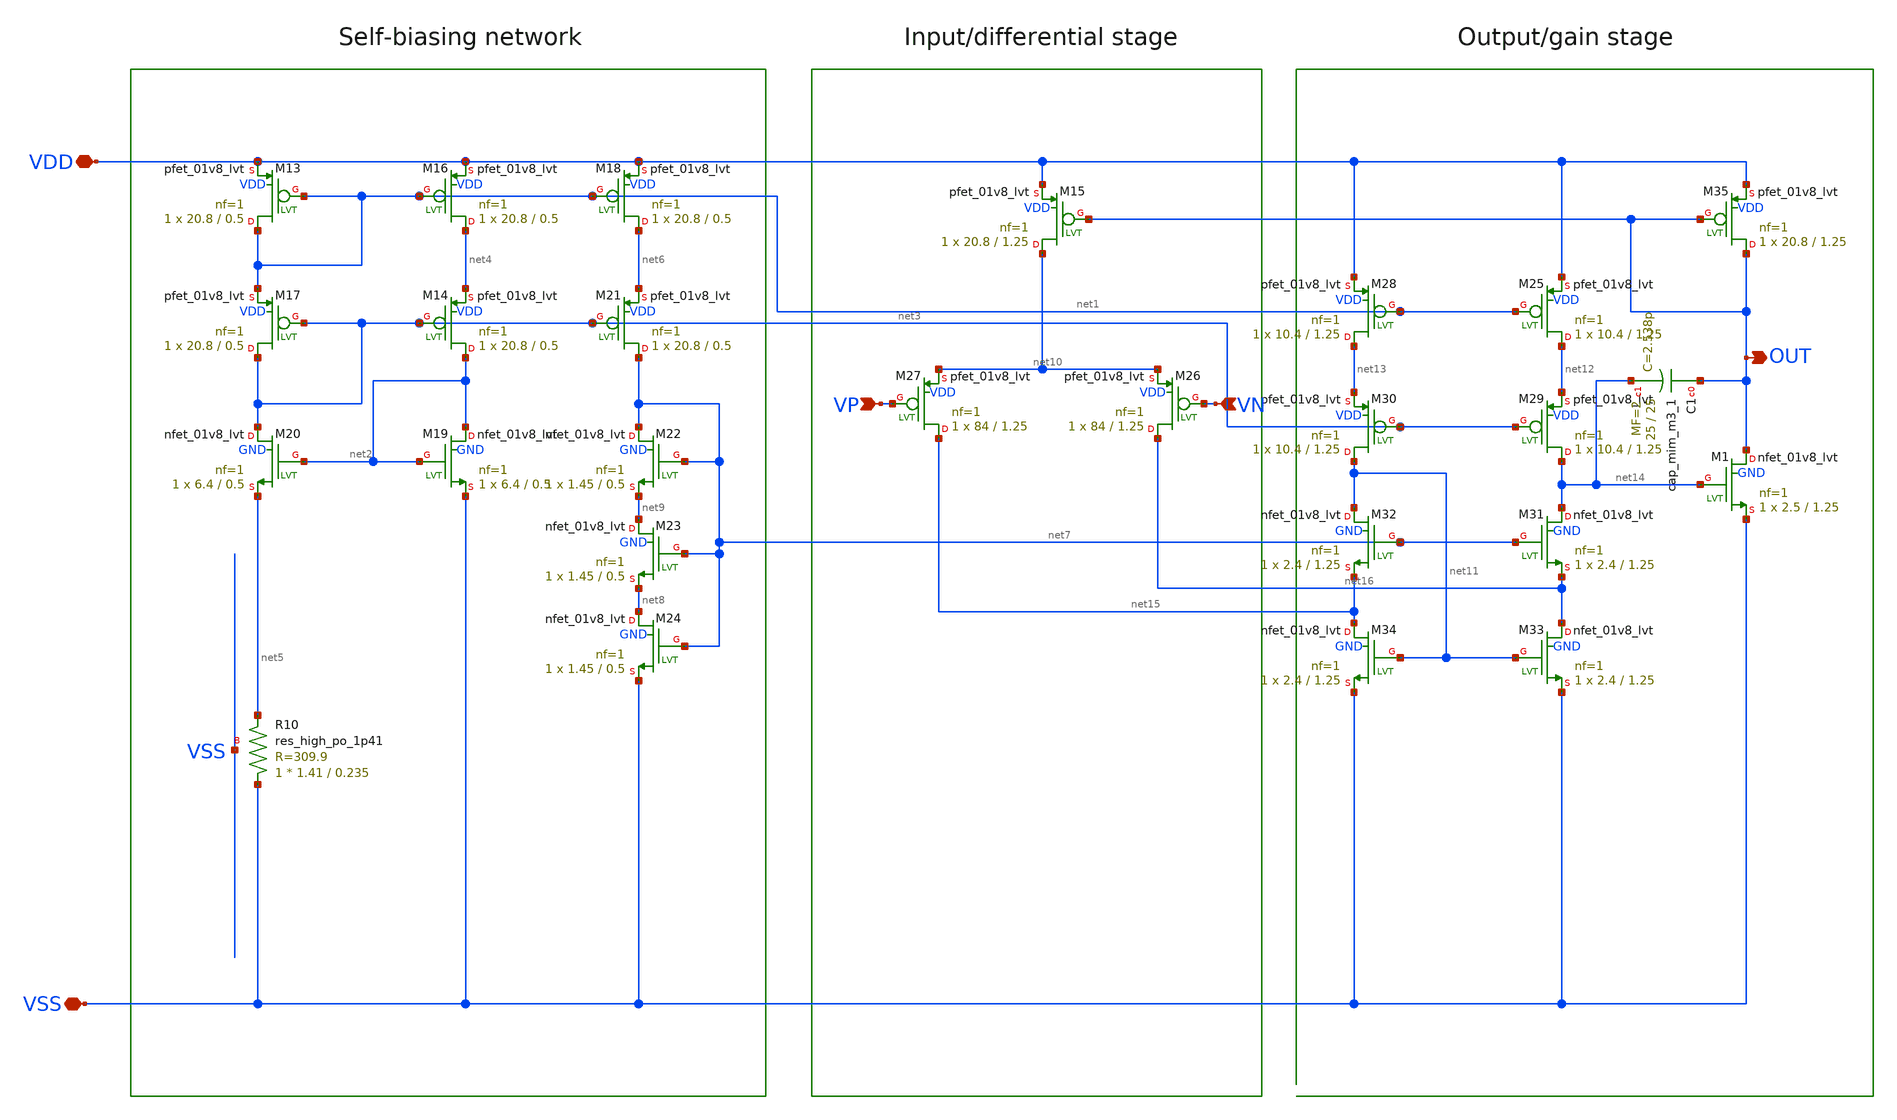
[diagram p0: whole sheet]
** sch_path: bandgap/bgr-opamp2/folded-cascode-opamp.sch
**.subckt folded-cascode-opamp VSS VDD VP VN OUT
*.iopin VSS
*.iopin VDD
*.ipin VP
*.ipin VN
*.opin OUT
XR10 VSS net5 VSS sky130_fd_pr__res_high_po_1p41 L=0.235 mult=1 m=1
XM19 net2 net2 VSS GND sky130_fd_pr__nfet_01v8_lvt L=0.5 W=6.4 nf=1 ad='int((nf+1)/2) * W/nf * 0.29'
+ as='int((nf+2)/2) * W/nf * 0.29' pd='2*int((nf+1)/2) * (W/nf + 0.29)' ps='2*int((nf+2)/2) * (W/nf + 0.29)'
+ nrd='0.29 / W' nrs='0.29 / W' sa=0 sb=0 sd=0 mult=1 m=1
XM20 net3 net2 net5 GND sky130_fd_pr__nfet_01v8_lvt L=0.5 W=6.4 nf=1 ad='int((nf+1)/2) * W/nf * 0.29'
+ as='int((nf+2)/2) * W/nf * 0.29' pd='2*int((nf+1)/2) * (W/nf + 0.29)' ps='2*int((nf+2)/2) * (W/nf + 0.29)'
+ nrd='0.29 / W' nrs='0.29 / W' sa=0 sb=0 sd=0 mult=1 m=1
XM16 net4 net1 VDD VDD sky130_fd_pr__pfet_01v8_lvt L=0.5 W=20.8 nf=1 ad='int((nf+1)/2) * W/nf * 0.29'
+ as='int((nf+2)/2) * W/nf * 0.29' pd='2*int((nf+1)/2) * (W/nf + 0.29)' ps='2*int((nf+2)/2) * (W/nf + 0.29)'
+ nrd='0.29 / W' nrs='0.29 / W' sa=0 sb=0 sd=0 mult=1 m=1
XM13 net1 net1 VDD VDD sky130_fd_pr__pfet_01v8_lvt L=0.5 W=20.8 nf=1 ad='int((nf+1)/2) * W/nf * 0.29'
+ as='int((nf+2)/2) * W/nf * 0.29' pd='2*int((nf+1)/2) * (W/nf + 0.29)' ps='2*int((nf+2)/2) * (W/nf + 0.29)'
+ nrd='0.29 / W' nrs='0.29 / W' sa=0 sb=0 sd=0 mult=1 m=1
XM14 net2 net3 net4 VDD sky130_fd_pr__pfet_01v8_lvt L=0.5 W=20.8 nf=1 ad='int((nf+1)/2) * W/nf * 0.29'
+ as='int((nf+2)/2) * W/nf * 0.29' pd='2*int((nf+1)/2) * (W/nf + 0.29)' ps='2*int((nf+2)/2) * (W/nf + 0.29)'
+ nrd='0.29 / W' nrs='0.29 / W' sa=0 sb=0 sd=0 mult=1 m=1
XM17 net3 net3 net1 VDD sky130_fd_pr__pfet_01v8_lvt L=0.5 W=20.8 nf=1 ad='int((nf+1)/2) * W/nf * 0.29'
+ as='int((nf+2)/2) * W/nf * 0.29' pd='2*int((nf+1)/2) * (W/nf + 0.29)' ps='2*int((nf+2)/2) * (W/nf + 0.29)'
+ nrd='0.29 / W' nrs='0.29 / W' sa=0 sb=0 sd=0 mult=1 m=1
XM18 net6 net1 VDD VDD sky130_fd_pr__pfet_01v8_lvt L=0.5 W=20.8 nf=1 ad='int((nf+1)/2) * W/nf * 0.29'
+ as='int((nf+2)/2) * W/nf * 0.29' pd='2*int((nf+1)/2) * (W/nf + 0.29)' ps='2*int((nf+2)/2) * (W/nf + 0.29)'
+ nrd='0.29 / W' nrs='0.29 / W' sa=0 sb=0 sd=0 mult=1 m=1
XM21 net7 net3 net6 VDD sky130_fd_pr__pfet_01v8_lvt L=0.5 W=20.8 nf=1 ad='int((nf+1)/2) * W/nf * 0.29'
+ as='int((nf+2)/2) * W/nf * 0.29' pd='2*int((nf+1)/2) * (W/nf + 0.29)' ps='2*int((nf+2)/2) * (W/nf + 0.29)'
+ nrd='0.29 / W' nrs='0.29 / W' sa=0 sb=0 sd=0 mult=1 m=1
XM22 net7 net7 net9 GND sky130_fd_pr__nfet_01v8_lvt L=0.5 W=1.45 nf=1 ad='int((nf+1)/2) * W/nf * 0.29'
+ as='int((nf+2)/2) * W/nf * 0.29' pd='2*int((nf+1)/2) * (W/nf + 0.29)' ps='2*int((nf+2)/2) * (W/nf + 0.29)'
+ nrd='0.29 / W' nrs='0.29 / W' sa=0 sb=0 sd=0 mult=1 m=1
XM23 net9 net7 net8 GND sky130_fd_pr__nfet_01v8_lvt L=0.5 W=1.45 nf=1 ad='int((nf+1)/2) * W/nf * 0.29'
+ as='int((nf+2)/2) * W/nf * 0.29' pd='2*int((nf+1)/2) * (W/nf + 0.29)' ps='2*int((nf+2)/2) * (W/nf + 0.29)'
+ nrd='0.29 / W' nrs='0.29 / W' sa=0 sb=0 sd=0 mult=1 m=1
XM24 net8 net7 VSS GND sky130_fd_pr__nfet_01v8_lvt L=0.5 W=1.45 nf=1 ad='int((nf+1)/2) * W/nf * 0.29'
+ as='int((nf+2)/2) * W/nf * 0.29' pd='2*int((nf+1)/2) * (W/nf + 0.29)' ps='2*int((nf+2)/2) * (W/nf + 0.29)'
+ nrd='0.29 / W' nrs='0.29 / W' sa=0 sb=0 sd=0 mult=1 m=1
XM26 net16 VN net10 VDD sky130_fd_pr__pfet_01v8_lvt L=1.25 W=84 nf=1 ad='int((nf+1)/2) * W/nf * 0.29'
+ as='int((nf+2)/2) * W/nf * 0.29' pd='2*int((nf+1)/2) * (W/nf + 0.29)' ps='2*int((nf+2)/2) * (W/nf + 0.29)'
+ nrd='0.29 / W' nrs='0.29 / W' sa=0 sb=0 sd=0 mult=1 m=1
XM27 net15 VP net10 VDD sky130_fd_pr__pfet_01v8_lvt L=1.25 W=84 nf=1 ad='int((nf+1)/2) * W/nf * 0.29'
+ as='int((nf+2)/2) * W/nf * 0.29' pd='2*int((nf+1)/2) * (W/nf + 0.29)' ps='2*int((nf+2)/2) * (W/nf + 0.29)'
+ nrd='0.29 / W' nrs='0.29 / W' sa=0 sb=0 sd=0 mult=1 m=1
XM15 net10 OUT VDD VDD sky130_fd_pr__pfet_01v8_lvt L=1.25 W=20.8 nf=1 ad='int((nf+1)/2) * W/nf * 0.29'
+ as='int((nf+2)/2) * W/nf * 0.29' pd='2*int((nf+1)/2) * (W/nf + 0.29)' ps='2*int((nf+2)/2) * (W/nf + 0.29)'
+ nrd='0.29 / W' nrs='0.29 / W' sa=0 sb=0 sd=0 mult=1 m=1
XM25 net12 net1 VDD VDD sky130_fd_pr__pfet_01v8_lvt L=1.25 W=10.4 nf=1 ad='int((nf+1)/2) * W/nf * 0.29'
+ as='int((nf+2)/2) * W/nf * 0.29' pd='2*int((nf+1)/2) * (W/nf + 0.29)' ps='2*int((nf+2)/2) * (W/nf + 0.29)'
+ nrd='0.29 / W' nrs='0.29 / W' sa=0 sb=0 sd=0 mult=1 m=1
XM28 net13 net1 VDD VDD sky130_fd_pr__pfet_01v8_lvt L=1.25 W=10.4 nf=1 ad='int((nf+1)/2) * W/nf * 0.29'
+ as='int((nf+2)/2) * W/nf * 0.29' pd='2*int((nf+1)/2) * (W/nf + 0.29)' ps='2*int((nf+2)/2) * (W/nf + 0.29)'
+ nrd='0.29 / W' nrs='0.29 / W' sa=0 sb=0 sd=0 mult=1 m=1
XM29 net14 net3 net12 VDD sky130_fd_pr__pfet_01v8_lvt L=1.25 W=10.4 nf=1 ad='int((nf+1)/2) * W/nf * 0.29'
+ as='int((nf+2)/2) * W/nf * 0.29' pd='2*int((nf+1)/2) * (W/nf + 0.29)' ps='2*int((nf+2)/2) * (W/nf + 0.29)'
+ nrd='0.29 / W' nrs='0.29 / W' sa=0 sb=0 sd=0 mult=1 m=1
XM30 net11 net3 net13 VDD sky130_fd_pr__pfet_01v8_lvt L=1.25 W=10.4 nf=1 ad='int((nf+1)/2) * W/nf * 0.29'
+ as='int((nf+2)/2) * W/nf * 0.29' pd='2*int((nf+1)/2) * (W/nf + 0.29)' ps='2*int((nf+2)/2) * (W/nf + 0.29)'
+ nrd='0.29 / W' nrs='0.29 / W' sa=0 sb=0 sd=0 mult=1 m=1
XM31 net14 net7 net16 GND sky130_fd_pr__nfet_01v8_lvt L=1.25 W=2.4 nf=1 ad='int((nf+1)/2) * W/nf * 0.29'
+ as='int((nf+2)/2) * W/nf * 0.29' pd='2*int((nf+1)/2) * (W/nf + 0.29)' ps='2*int((nf+2)/2) * (W/nf + 0.29)'
+ nrd='0.29 / W' nrs='0.29 / W' sa=0 sb=0 sd=0 mult=1 m=1
XM32 net11 net7 net15 GND sky130_fd_pr__nfet_01v8_lvt L=1.25 W=2.4 nf=1 ad='int((nf+1)/2) * W/nf * 0.29'
+ as='int((nf+2)/2) * W/nf * 0.29' pd='2*int((nf+1)/2) * (W/nf + 0.29)' ps='2*int((nf+2)/2) * (W/nf + 0.29)'
+ nrd='0.29 / W' nrs='0.29 / W' sa=0 sb=0 sd=0 mult=1 m=1
XM33 net16 net11 VSS GND sky130_fd_pr__nfet_01v8_lvt L=1.25 W=2.4 nf=1 ad='int((nf+1)/2) * W/nf * 0.29'
+ as='int((nf+2)/2) * W/nf * 0.29' pd='2*int((nf+1)/2) * (W/nf + 0.29)' ps='2*int((nf+2)/2) * (W/nf + 0.29)'
+ nrd='0.29 / W' nrs='0.29 / W' sa=0 sb=0 sd=0 mult=1 m=1
XM34 net15 net11 VSS GND sky130_fd_pr__nfet_01v8_lvt L=1.25 W=2.4 nf=1 ad='int((nf+1)/2) * W/nf * 0.29'
+ as='int((nf+2)/2) * W/nf * 0.29' pd='2*int((nf+1)/2) * (W/nf + 0.29)' ps='2*int((nf+2)/2) * (W/nf + 0.29)'
+ nrd='0.29 / W' nrs='0.29 / W' sa=0 sb=0 sd=0 mult=1 m=1
XM35 OUT OUT VDD VDD sky130_fd_pr__pfet_01v8_lvt L=1.25 W=20.8 nf=1 ad='int((nf+1)/2) * W/nf * 0.29'
+ as='int((nf+2)/2) * W/nf * 0.29' pd='2*int((nf+1)/2) * (W/nf + 0.29)' ps='2*int((nf+2)/2) * (W/nf + 0.29)'
+ nrd='0.29 / W' nrs='0.29 / W' sa=0 sb=0 sd=0 mult=1 m=1
XM1 OUT net14 VSS GND sky130_fd_pr__nfet_01v8_lvt L=1.25 W=2.5 nf=1 ad='int((nf+1)/2) * W/nf * 0.29'
+ as='int((nf+2)/2) * W/nf * 0.29' pd='2*int((nf+1)/2) * (W/nf + 0.29)' ps='2*int((nf+2)/2) * (W/nf + 0.29)'
+ nrd='0.29 / W' nrs='0.29 / W' sa=0 sb=0 sd=0 mult=1 m=1
XC1 OUT net14 sky130_fd_pr__cap_mim_m3_1 W=25 L=25 MF=2 m=2
**.ends
.end
